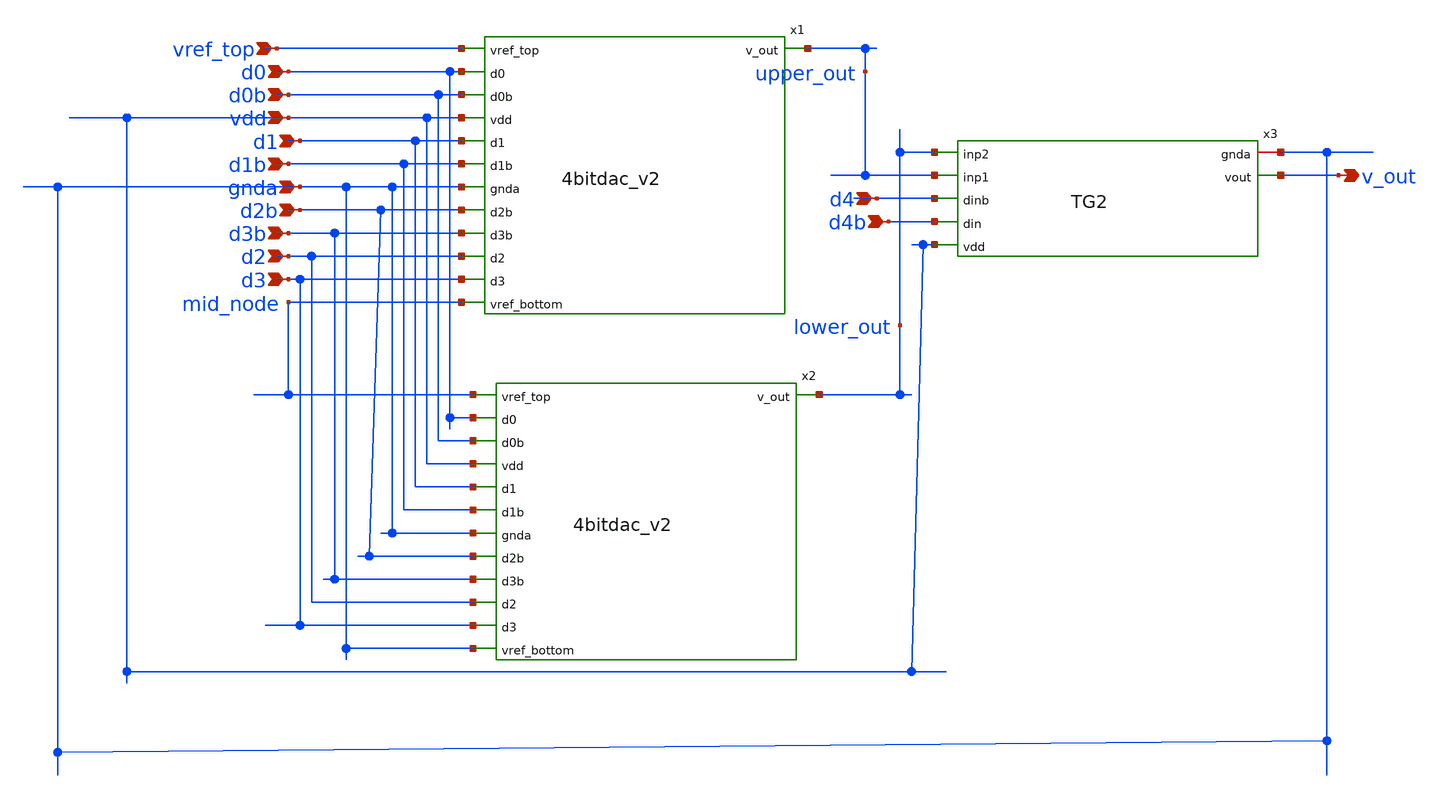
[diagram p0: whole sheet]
** sch_path: prelayout/5bitdac.sch
**.subckt 5bitdac vref_top d0 vdd d1b d0b d1 gnda d2b d3b d2 d3 d4 d4b v_out
*.ipin vref_top
*.ipin d0
*.ipin vdd
*.ipin d1b
*.ipin d0b
*.ipin d1
*.ipin gnda
*.ipin d2b
*.ipin d3b
*.ipin d2
*.ipin d3
*.ipin d4
*.ipin d4b
*.opin v_out
Xx3 gnda v_out lower_out upper_out d4 d4b vdd TG2
x1 vref_top d0 d0b vdd d1 d1b gnda upper_out d2b d3b d2 d3 mid_node 4bitdac_v2
x2 mid_node d0 d0b vdd d1 d1b gnda lower_out d2b d3b d2 d3 gnda 4bitdac_v2
**.ends
.end
